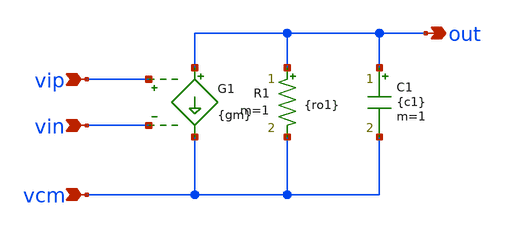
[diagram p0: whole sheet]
** sch_path: modules/ideal_op_single.sch
**.subckt ideal_op_single vip vin out vcm
*.ipin vip
*.ipin vin
*.opin out
*.ipin vcm
G1 out vcm vip vin {gm}
R1 out vcm {ro1} m=1
C1 out vcm {c1} m=1
**.ends
.end
